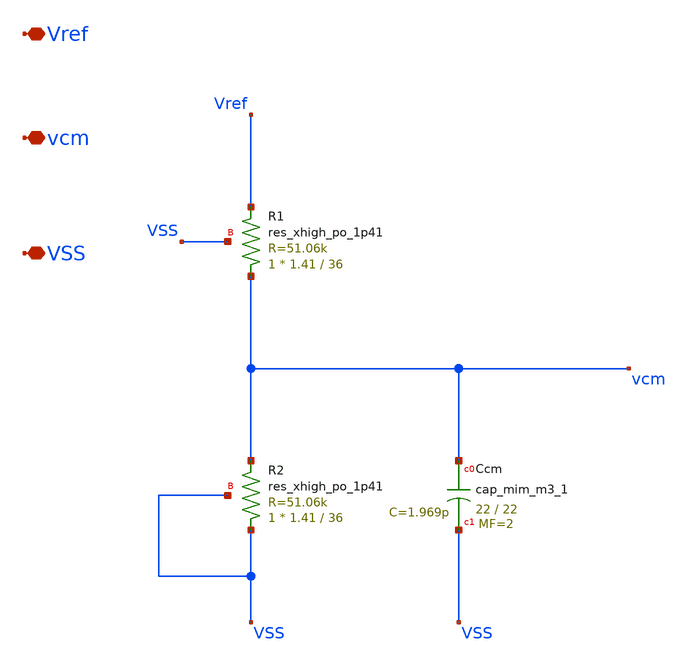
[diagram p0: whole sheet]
** sch_path: xschem/vcm_gen.sch
**.subckt vcm_gen Vref vcm VSS
*.iopin Vref
*.iopin vcm
*.iopin VSS
XR1 vcm Vref VSS sky130_fd_pr__res_xhigh_po_1p41 L=36 mult=1 m=1
XR2 VSS vcm VSS sky130_fd_pr__res_xhigh_po_1p41 L=36 mult=1 m=1
XCcm vcm VSS sky130_fd_pr__cap_mim_m3_1 W=22 L=22 MF=2 m=2
**.ends
.end
